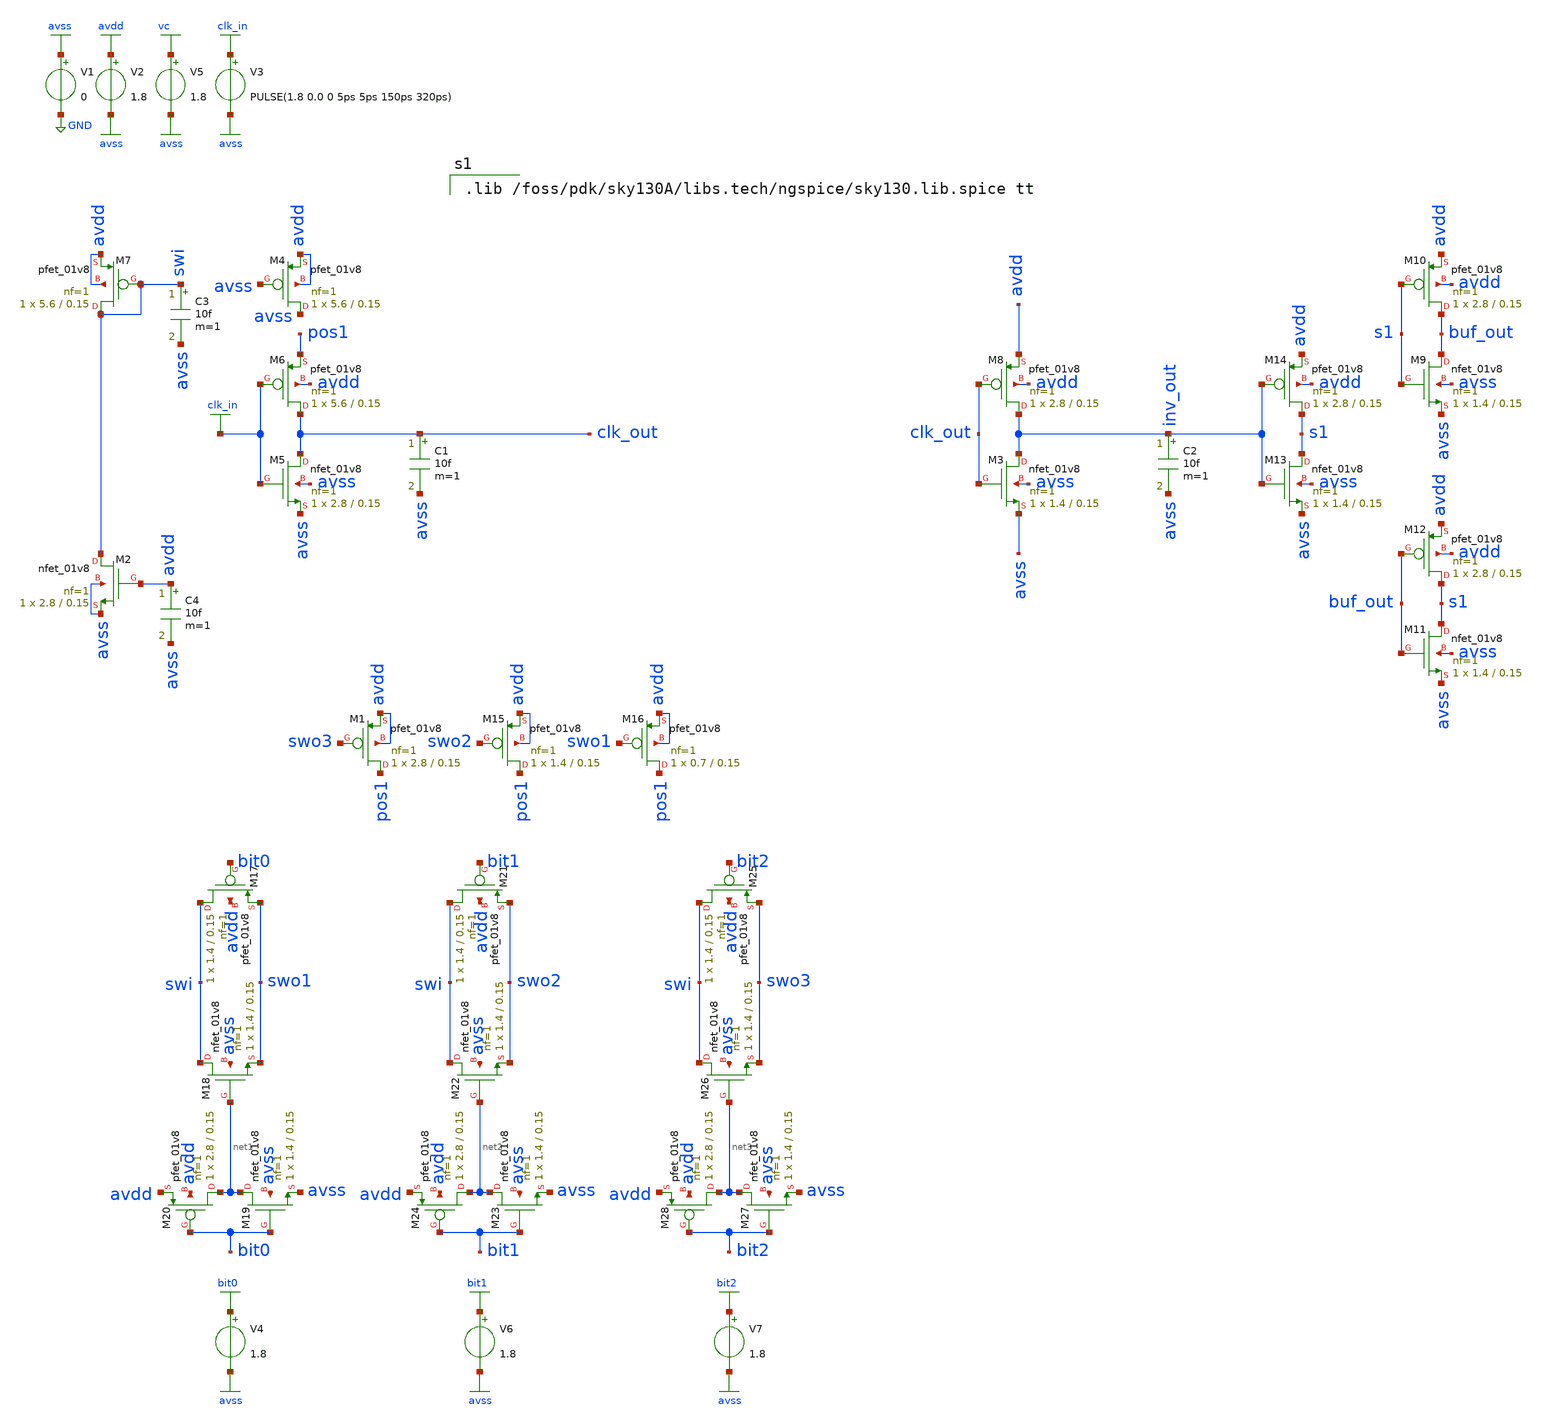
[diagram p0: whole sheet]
** sch_path: slopebuf_sim3.sch
**.subckt slopebuf_sim3
V1 avss GND 0
V2 avdd avss 1.8
V3 clk_in avss PULSE(1.8 0.0 0 5ps 5ps 150ps 320ps)
V5 vc avss 1.8
XM5 clk_out clk_in avss avss sky130_fd_pr__nfet_01v8 L=0.15 W=2.8 nf=1 ad='int((nf+1)/2) * W/nf * 0.29'
+ as='int((nf+2)/2) * W/nf * 0.29' pd='2*int((nf+1)/2) * (W/nf + 0.29)' ps='2*int((nf+2)/2) * (W/nf + 0.29)'
+ nrd='0.29 / W' nrs='0.29 / W' sa=0 sb=0 sd=0 mult=1 m=1
XM6 clk_out clk_in pos1 avdd sky130_fd_pr__pfet_01v8 L=0.15 W=5.6 nf=1 ad='int((nf+1)/2) * W/nf * 0.29'
+ as='int((nf+2)/2) * W/nf * 0.29' pd='2*int((nf+1)/2) * (W/nf + 0.29)' ps='2*int((nf+2)/2) * (W/nf + 0.29)'
+ nrd='0.29 / W' nrs='0.29 / W' sa=0 sb=0 sd=0 mult=1 m=1
XM4 avss avss avdd avdd sky130_fd_pr__pfet_01v8 L=0.15 W=5.6 nf=1 ad='int((nf+1)/2) * W/nf * 0.29' as='int((nf+2)/2) * W/nf * 0.29'
+ pd='2*int((nf+1)/2) * (W/nf + 0.29)' ps='2*int((nf+2)/2) * (W/nf + 0.29)' nrd='0.29 / W' nrs='0.29 / W'
+ sa=0 sb=0 sd=0 mult=1 m=1
XM7 swi swi avdd avdd sky130_fd_pr__pfet_01v8 L=0.15 W=5.6 nf=1 ad='int((nf+1)/2) * W/nf * 0.29' as='int((nf+2)/2) * W/nf * 0.29'
+ pd='2*int((nf+1)/2) * (W/nf + 0.29)' ps='2*int((nf+2)/2) * (W/nf + 0.29)' nrd='0.29 / W' nrs='0.29 / W'
+ sa=0 sb=0 sd=0 mult=1 m=1
C1 clk_out avss 10f m=1
XM2 swi avdd avss avss sky130_fd_pr__nfet_01v8 L=0.15 W=2.8 nf=1 ad='int((nf+1)/2) * W/nf * 0.29' as='int((nf+2)/2) * W/nf * 0.29'
+ pd='2*int((nf+1)/2) * (W/nf + 0.29)' ps='2*int((nf+2)/2) * (W/nf + 0.29)' nrd='0.29 / W' nrs='0.29 / W'
+ sa=0 sb=0 sd=0 mult=1 m=1
XM3 inv_out clk_out avss avss sky130_fd_pr__nfet_01v8 L=0.15 W=1.4 nf=1 ad='int((nf+1)/2) * W/nf * 0.29'
+ as='int((nf+2)/2) * W/nf * 0.29' pd='2*int((nf+1)/2) * (W/nf + 0.29)' ps='2*int((nf+2)/2) * (W/nf + 0.29)'
+ nrd='0.29 / W' nrs='0.29 / W' sa=0 sb=0 sd=0 mult=1 m=1
XM8 inv_out clk_out avdd avdd sky130_fd_pr__pfet_01v8 L=0.15 W=2.8 nf=1 ad='int((nf+1)/2) * W/nf * 0.29'
+ as='int((nf+2)/2) * W/nf * 0.29' pd='2*int((nf+1)/2) * (W/nf + 0.29)' ps='2*int((nf+2)/2) * (W/nf + 0.29)'
+ nrd='0.29 / W' nrs='0.29 / W' sa=0 sb=0 sd=0 mult=1 m=1
C2 inv_out avss 10f m=1
C3 swi avss 10f m=1
XM9 buf_out s1 avss avss sky130_fd_pr__nfet_01v8 L=0.15 W=1.4 nf=1 ad='int((nf+1)/2) * W/nf * 0.29' as='int((nf+2)/2) * W/nf * 0.29'
+ pd='2*int((nf+1)/2) * (W/nf + 0.29)' ps='2*int((nf+2)/2) * (W/nf + 0.29)' nrd='0.29 / W' nrs='0.29 / W'
+ sa=0 sb=0 sd=0 mult=1 m=1
XM10 buf_out s1 avdd avdd sky130_fd_pr__pfet_01v8 L=0.15 W=2.8 nf=1 ad='int((nf+1)/2) * W/nf * 0.29'
+ as='int((nf+2)/2) * W/nf * 0.29' pd='2*int((nf+1)/2) * (W/nf + 0.29)' ps='2*int((nf+2)/2) * (W/nf + 0.29)'
+ nrd='0.29 / W' nrs='0.29 / W' sa=0 sb=0 sd=0 mult=1 m=1
XM11 s1 buf_out avss avss sky130_fd_pr__nfet_01v8 L=0.15 W=1.4 nf=1 ad='int((nf+1)/2) * W/nf * 0.29'
+ as='int((nf+2)/2) * W/nf * 0.29' pd='2*int((nf+1)/2) * (W/nf + 0.29)' ps='2*int((nf+2)/2) * (W/nf + 0.29)'
+ nrd='0.29 / W' nrs='0.29 / W' sa=0 sb=0 sd=0 mult=1 m=1
XM12 s1 buf_out avdd avdd sky130_fd_pr__pfet_01v8 L=0.15 W=2.8 nf=1 ad='int((nf+1)/2) * W/nf * 0.29'
+ as='int((nf+2)/2) * W/nf * 0.29' pd='2*int((nf+1)/2) * (W/nf + 0.29)' ps='2*int((nf+2)/2) * (W/nf + 0.29)'
+ nrd='0.29 / W' nrs='0.29 / W' sa=0 sb=0 sd=0 mult=1 m=1
C4 avdd avss 10f m=1
XM13 s1 inv_out avss avss sky130_fd_pr__nfet_01v8 L=0.15 W=1.4 nf=1 ad='int((nf+1)/2) * W/nf * 0.29'
+ as='int((nf+2)/2) * W/nf * 0.29' pd='2*int((nf+1)/2) * (W/nf + 0.29)' ps='2*int((nf+2)/2) * (W/nf + 0.29)'
+ nrd='0.29 / W' nrs='0.29 / W' sa=0 sb=0 sd=0 mult=1 m=1
XM14 s1 inv_out avdd avdd sky130_fd_pr__pfet_01v8 L=0.15 W=2.8 nf=1 ad='int((nf+1)/2) * W/nf * 0.29'
+ as='int((nf+2)/2) * W/nf * 0.29' pd='2*int((nf+1)/2) * (W/nf + 0.29)' ps='2*int((nf+2)/2) * (W/nf + 0.29)'
+ nrd='0.29 / W' nrs='0.29 / W' sa=0 sb=0 sd=0 mult=1 m=1
XM1 pos1 swo3 avdd avdd sky130_fd_pr__pfet_01v8 L=0.15 W=2.8 nf=1 ad='int((nf+1)/2) * W/nf * 0.29' as='int((nf+2)/2) * W/nf * 0.29'
+ pd='2*int((nf+1)/2) * (W/nf + 0.29)' ps='2*int((nf+2)/2) * (W/nf + 0.29)' nrd='0.29 / W' nrs='0.29 / W'
+ sa=0 sb=0 sd=0 mult=1 m=1
XM15 pos1 swo2 avdd avdd sky130_fd_pr__pfet_01v8 L=0.15 W=1.4 nf=1 ad='int((nf+1)/2) * W/nf * 0.29' as='int((nf+2)/2) * W/nf * 0.29'
+ pd='2*int((nf+1)/2) * (W/nf + 0.29)' ps='2*int((nf+2)/2) * (W/nf + 0.29)' nrd='0.29 / W' nrs='0.29 / W'
+ sa=0 sb=0 sd=0 mult=1 m=1
XM16 pos1 swo1 avdd avdd sky130_fd_pr__pfet_01v8 L=0.15 W=0.7 nf=1 ad='int((nf+1)/2) * W/nf * 0.29' as='int((nf+2)/2) * W/nf * 0.29'
+ pd='2*int((nf+1)/2) * (W/nf + 0.29)' ps='2*int((nf+2)/2) * (W/nf + 0.29)' nrd='0.29 / W' nrs='0.29 / W'
+ sa=0 sb=0 sd=0 mult=1 m=1
XM17 swi bit0 swo1 avdd sky130_fd_pr__pfet_01v8 L=0.15 W=1.4 nf=1 ad='int((nf+1)/2) * W/nf * 0.29' as='int((nf+2)/2) * W/nf * 0.29'
+ pd='2*int((nf+1)/2) * (W/nf + 0.29)' ps='2*int((nf+2)/2) * (W/nf + 0.29)' nrd='0.29 / W' nrs='0.29 / W'
+ sa=0 sb=0 sd=0 mult=1 m=1
XM18 swi net1 swo1 avss sky130_fd_pr__nfet_01v8 L=0.15 W=1.4 nf=1 ad='int((nf+1)/2) * W/nf * 0.29' as='int((nf+2)/2) * W/nf * 0.29'
+ pd='2*int((nf+1)/2) * (W/nf + 0.29)' ps='2*int((nf+2)/2) * (W/nf + 0.29)' nrd='0.29 / W' nrs='0.29 / W'
+ sa=0 sb=0 sd=0 mult=1 m=1
XM19 net1 bit0 avss avss sky130_fd_pr__nfet_01v8 L=0.15 W=1.4 nf=1 ad='int((nf+1)/2) * W/nf * 0.29' as='int((nf+2)/2) * W/nf * 0.29'
+ pd='2*int((nf+1)/2) * (W/nf + 0.29)' ps='2*int((nf+2)/2) * (W/nf + 0.29)' nrd='0.29 / W' nrs='0.29 / W'
+ sa=0 sb=0 sd=0 mult=1 m=1
XM20 net1 bit0 avdd avdd sky130_fd_pr__pfet_01v8 L=0.15 W=2.8 nf=1 ad='int((nf+1)/2) * W/nf * 0.29' as='int((nf+2)/2) * W/nf * 0.29'
+ pd='2*int((nf+1)/2) * (W/nf + 0.29)' ps='2*int((nf+2)/2) * (W/nf + 0.29)' nrd='0.29 / W' nrs='0.29 / W'
+ sa=0 sb=0 sd=0 mult=1 m=1
XM21 swi bit1 swo2 avdd sky130_fd_pr__pfet_01v8 L=0.15 W=1.4 nf=1 ad='int((nf+1)/2) * W/nf * 0.29' as='int((nf+2)/2) * W/nf * 0.29'
+ pd='2*int((nf+1)/2) * (W/nf + 0.29)' ps='2*int((nf+2)/2) * (W/nf + 0.29)' nrd='0.29 / W' nrs='0.29 / W'
+ sa=0 sb=0 sd=0 mult=1 m=1
XM22 swi net2 swo2 avss sky130_fd_pr__nfet_01v8 L=0.15 W=1.4 nf=1 ad='int((nf+1)/2) * W/nf * 0.29' as='int((nf+2)/2) * W/nf * 0.29'
+ pd='2*int((nf+1)/2) * (W/nf + 0.29)' ps='2*int((nf+2)/2) * (W/nf + 0.29)' nrd='0.29 / W' nrs='0.29 / W'
+ sa=0 sb=0 sd=0 mult=1 m=1
XM23 net2 bit1 avss avss sky130_fd_pr__nfet_01v8 L=0.15 W=1.4 nf=1 ad='int((nf+1)/2) * W/nf * 0.29' as='int((nf+2)/2) * W/nf * 0.29'
+ pd='2*int((nf+1)/2) * (W/nf + 0.29)' ps='2*int((nf+2)/2) * (W/nf + 0.29)' nrd='0.29 / W' nrs='0.29 / W'
+ sa=0 sb=0 sd=0 mult=1 m=1
XM24 net2 bit1 avdd avdd sky130_fd_pr__pfet_01v8 L=0.15 W=2.8 nf=1 ad='int((nf+1)/2) * W/nf * 0.29' as='int((nf+2)/2) * W/nf * 0.29'
+ pd='2*int((nf+1)/2) * (W/nf + 0.29)' ps='2*int((nf+2)/2) * (W/nf + 0.29)' nrd='0.29 / W' nrs='0.29 / W'
+ sa=0 sb=0 sd=0 mult=1 m=1
XM25 swi bit2 swo3 avdd sky130_fd_pr__pfet_01v8 L=0.15 W=1.4 nf=1 ad='int((nf+1)/2) * W/nf * 0.29' as='int((nf+2)/2) * W/nf * 0.29'
+ pd='2*int((nf+1)/2) * (W/nf + 0.29)' ps='2*int((nf+2)/2) * (W/nf + 0.29)' nrd='0.29 / W' nrs='0.29 / W'
+ sa=0 sb=0 sd=0 mult=1 m=1
XM26 swi net3 swo3 avss sky130_fd_pr__nfet_01v8 L=0.15 W=1.4 nf=1 ad='int((nf+1)/2) * W/nf * 0.29' as='int((nf+2)/2) * W/nf * 0.29'
+ pd='2*int((nf+1)/2) * (W/nf + 0.29)' ps='2*int((nf+2)/2) * (W/nf + 0.29)' nrd='0.29 / W' nrs='0.29 / W'
+ sa=0 sb=0 sd=0 mult=1 m=1
XM27 net3 bit2 avss avss sky130_fd_pr__nfet_01v8 L=0.15 W=1.4 nf=1 ad='int((nf+1)/2) * W/nf * 0.29' as='int((nf+2)/2) * W/nf * 0.29'
+ pd='2*int((nf+1)/2) * (W/nf + 0.29)' ps='2*int((nf+2)/2) * (W/nf + 0.29)' nrd='0.29 / W' nrs='0.29 / W'
+ sa=0 sb=0 sd=0 mult=1 m=1
XM28 net3 bit2 avdd avdd sky130_fd_pr__pfet_01v8 L=0.15 W=2.8 nf=1 ad='int((nf+1)/2) * W/nf * 0.29' as='int((nf+2)/2) * W/nf * 0.29'
+ pd='2*int((nf+1)/2) * (W/nf + 0.29)' ps='2*int((nf+2)/2) * (W/nf + 0.29)' nrd='0.29 / W' nrs='0.29 / W'
+ sa=0 sb=0 sd=0 mult=1 m=1
V4 bit0 avss 1.8
V6 bit1 avss 1.8
V7 bit2 avss 1.8
**** begin user architecture code

.lib /foss/pdk/sky130A/libs.tech/ngspice/sky130.lib.spice tt












.control
alter v4 0
alter v6 0
alter v7 0
save clk_in clk_out @V1[i]
tran 0.01n 50n 20n
run
plot clk_out clk_in
*plot tran1.clk_out tran2.clk_out tran3.clk_out tran4.clk_out tran5.clk_out tran6.clk_out
*+ tran7.clk_out tran8.clk_out xlimit 49ns 50ns
*plot tran1.s1 tran2.s1 tran3.s1 tran4.s1 tran5.s1 tran6.s1 tran7.s1 tran8.s1 tran9.s1 tran10.s1
*+ xlimit 49ns 50ns
*plot tran1.@V1[i] tran5.@V1[i] tran10.@V1[i]
.endc
.end


**** end user architecture code
**.ends
.GLOBAL avdd
.GLOBAL avss
.GLOBAL GND
.GLOBAL vc
.GLOBAL clk_in
.GLOBAL bit0
.GLOBAL bit1
.GLOBAL bit2
.end
